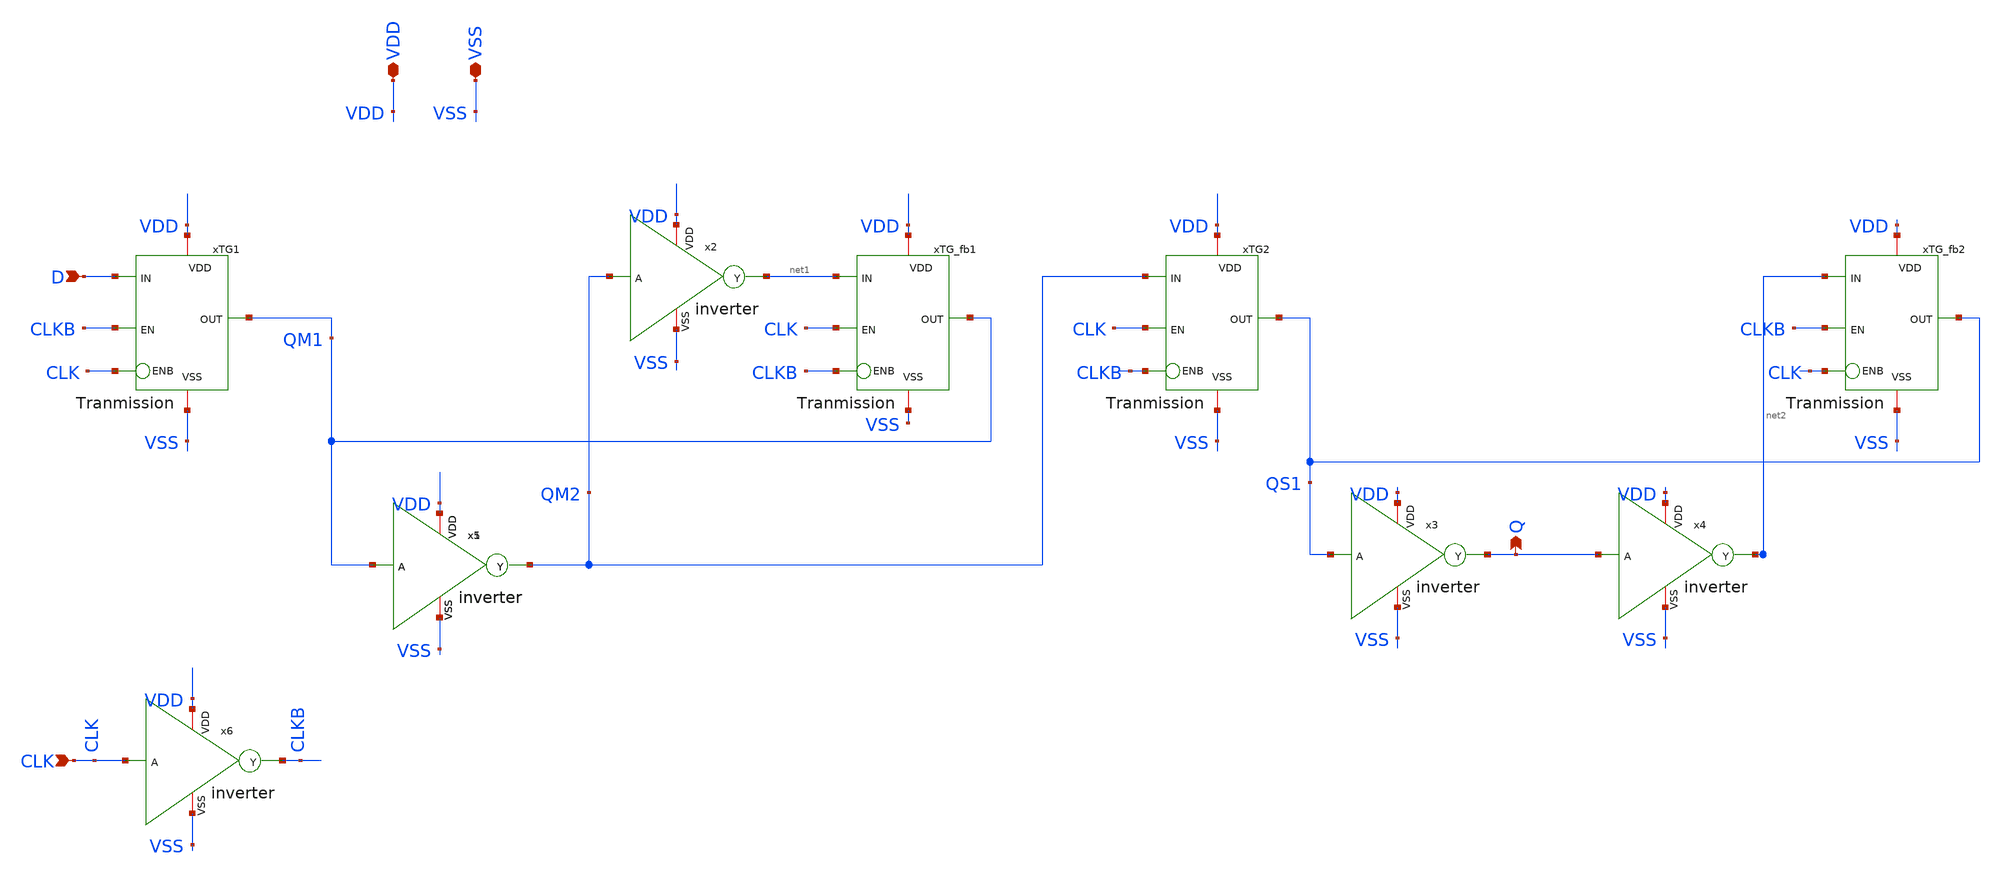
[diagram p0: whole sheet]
** sch_path: LogicGate/D_FlipFlop.sch
**.subckt D_FlipFlop D CLK Q VDD VSS
*.ipin D
*.ipin CLK
*.opin Q
*.iopin VDD
*.iopin VSS
xTG1 VDD CLK QM1 D CLKB VSS Tranmission
xTG2 VDD CLKB QS1 QM2 CLK VSS Tranmission
xTG_fb1 VDD CLKB QM1 net1 CLK VSS Tranmission
xTG_fb2 VDD CLK QS1 net2 CLKB VSS Tranmission
x1 VDD QM1 QM2 VSS inverter
x2 VDD QM2 net1 VSS inverter
x3 VDD QS1 Q VSS inverter
x4 VDD Q net2 VSS inverter
x5 VDD QM1 QM2 VSS inverter
x6 VDD CLK CLKB VSS inverter
**.ends

* expanding   symbol:  /foss/designs/LogicGate/Tranmission.sym # of pins=6
** sym_path: LogicGate/Tranmission.sym
** sch_path: LogicGate/Tranmission.sch
.subckt Tranmission VDD ENB OUT IN EN VSS
*.ipin IN
*.opin OUT
*.iopin VDD
*.iopin VSS
*.ipin EN
*.ipin ENB
XXM1 OUT ENB IN VDD sg13_lv_pmos w=0.15u l=0.13u ng=1 m=1 mm_ok=1
XXM2 OUT EN IN VSS sg13_lv_nmos w=0.15u l=0.13u ng=1 m=1 mm_ok=1
.ends


* expanding   symbol:  /foss/designs/BTDay6-Ex/inverter.sym # of pins=4
** sym_path: BTDay6-Ex/inverter.sym
** sch_path: BTDay6-Ex/inverter.sch
.subckt inverter VDD A Y VSS
*.ipin A
*.opin Y
*.iopin VDD
*.iopin VSS
XM1 Y A VSS VSS sg13_lv_nmos w=0.15u l=0.13u ng=1 m=1 mm_ok=1
XM2 Y A VDD VDD sg13_lv_pmos w=0.15u l=0.13u ng=1 m=1 mm_ok=1
.ends

.end
